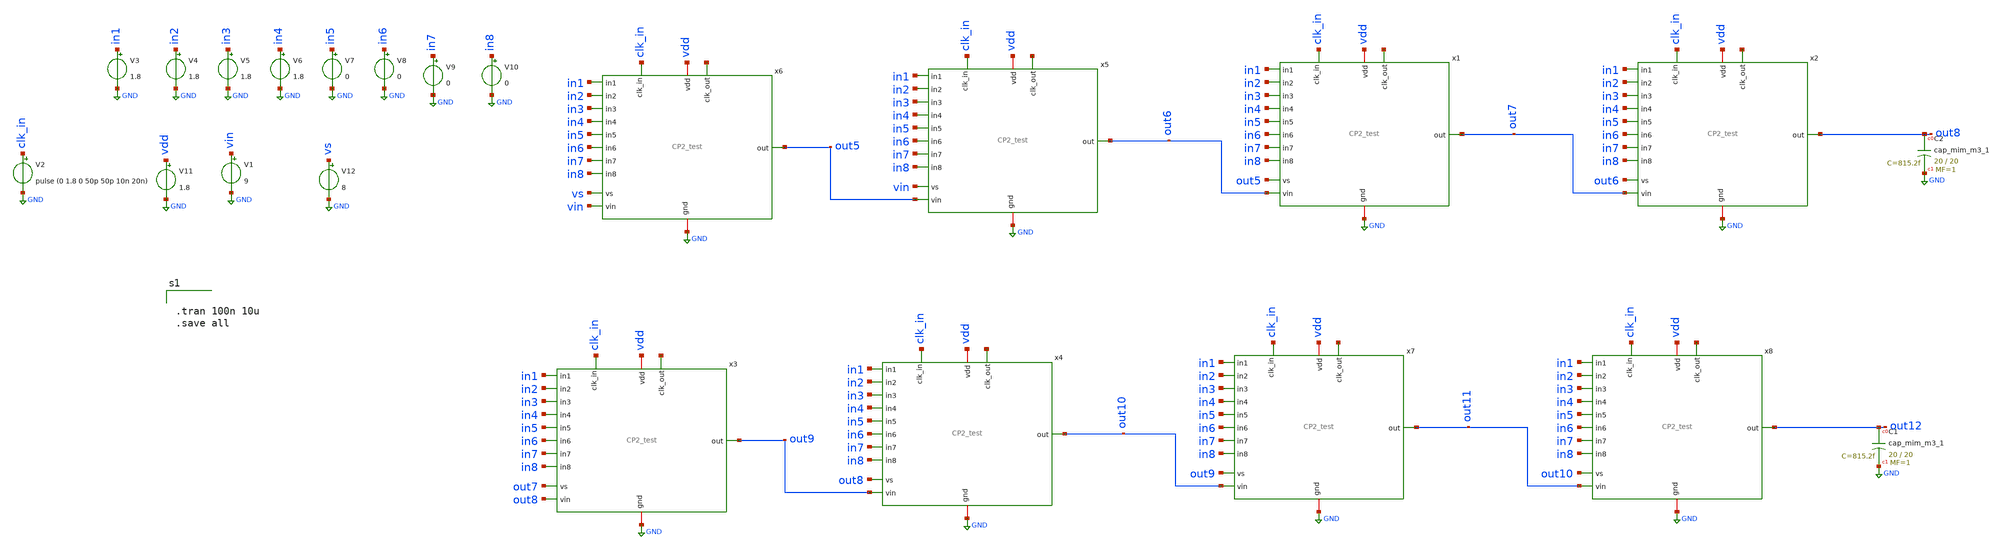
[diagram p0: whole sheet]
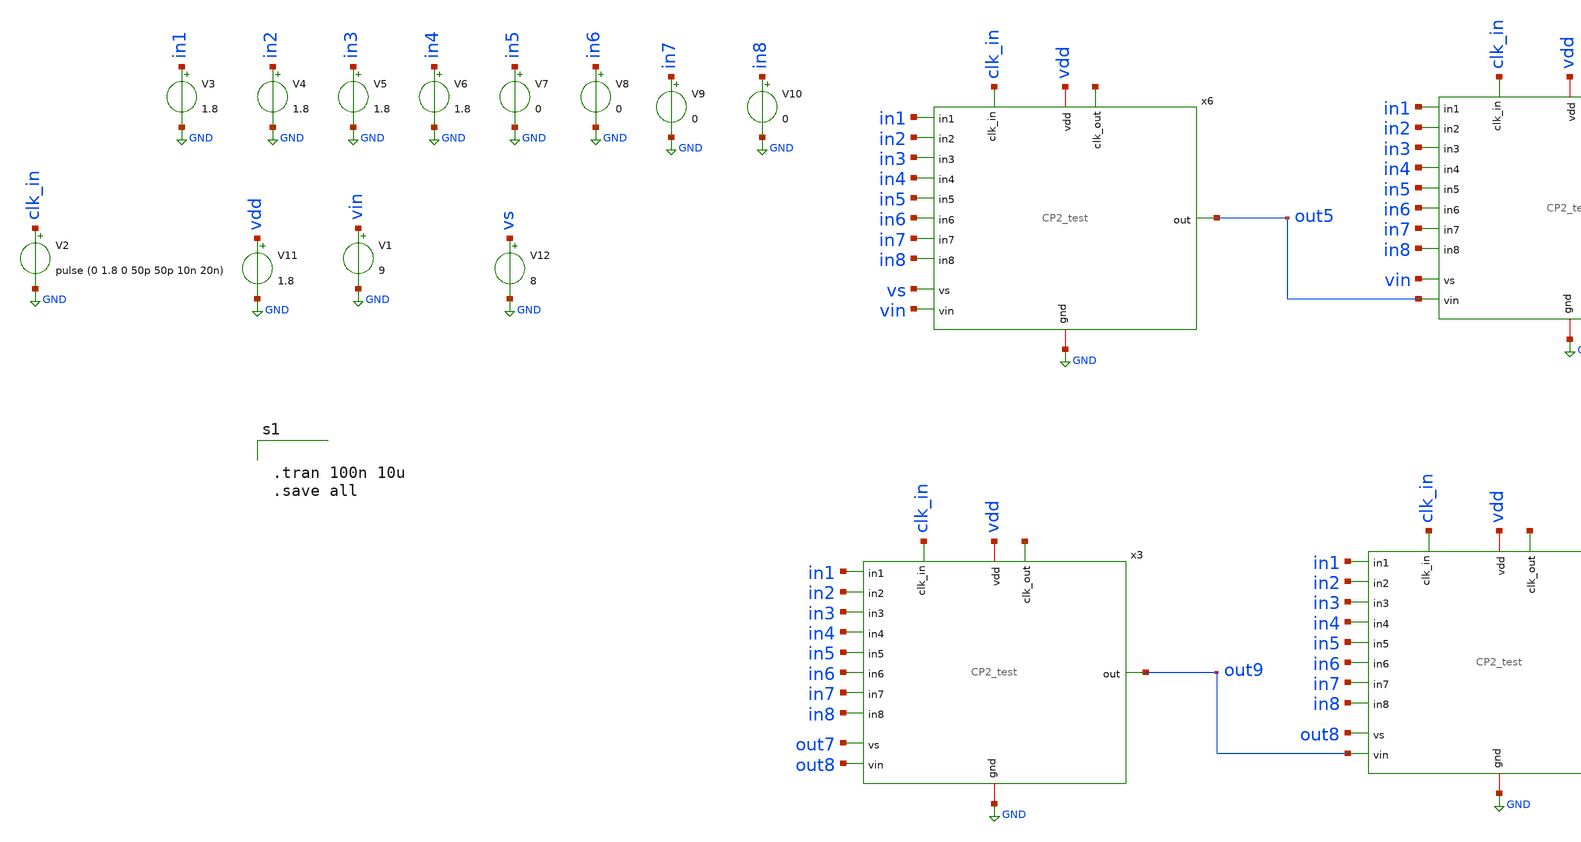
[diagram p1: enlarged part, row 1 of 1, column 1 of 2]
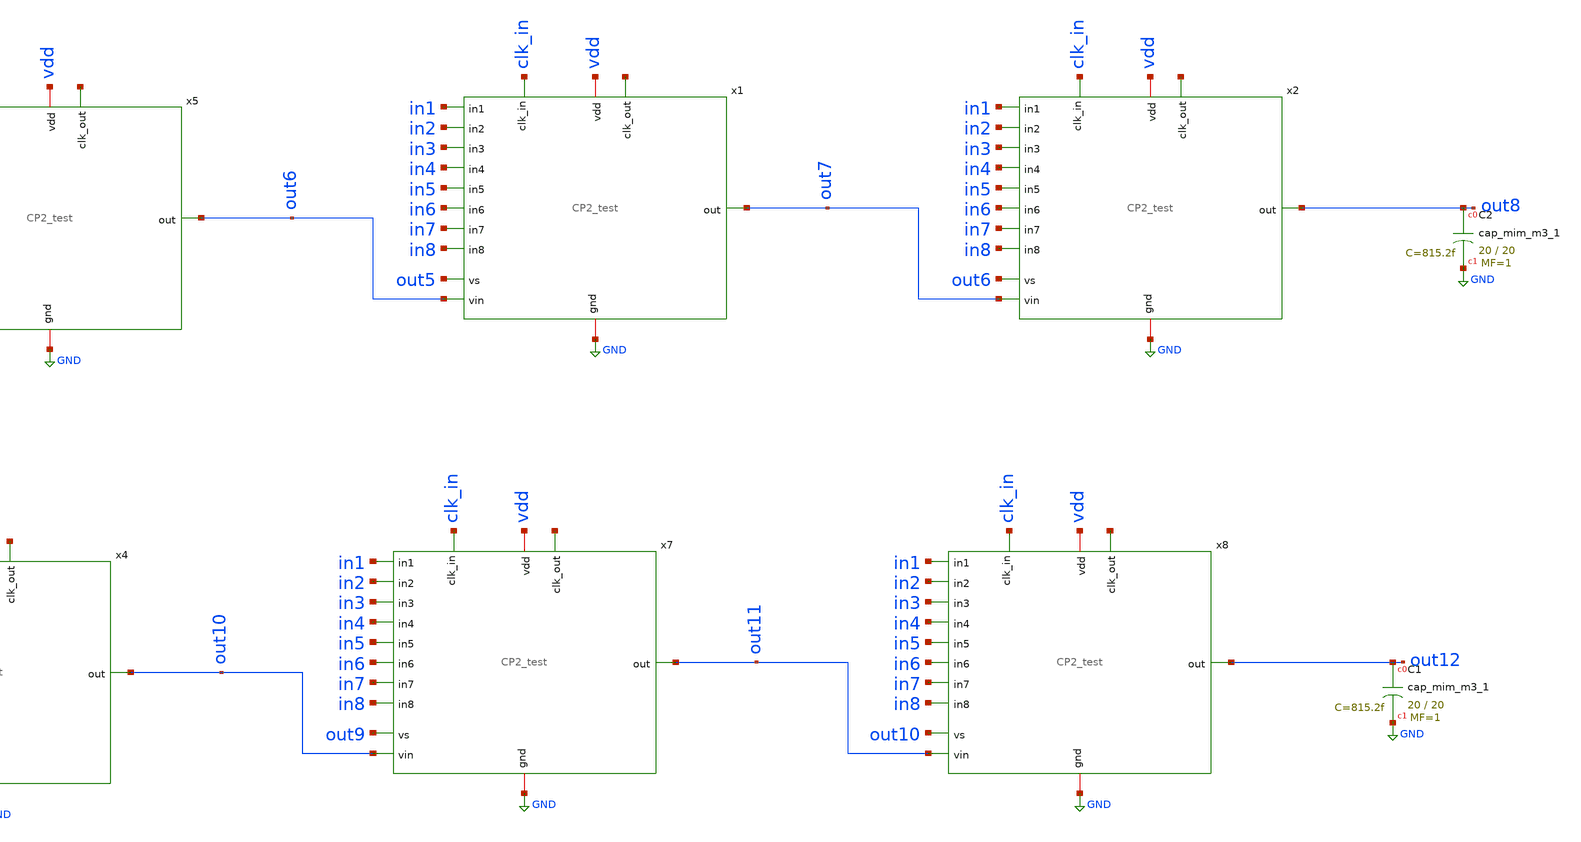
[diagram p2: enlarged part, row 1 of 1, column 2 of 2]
** sch_path: xschem/charge_pumps2/CP2_tb.sch
**.subckt CP2_tb
V1 vin GND 9
V2 clk_in GND pulse (0 1.8 0 50p 50p 10n 20n)
V3 in1 GND 1.8
V4 in2 GND 1.8
V5 in3 GND 1.8
V6 in4 GND 1.8
V7 in5 GND 0
V8 in6 GND 0
V9 in7 GND 0
V10 in8 GND 0
V11 vdd GND 1.8
x6 GND vs clk_in vin out5 in1 in2 in3 in4 in5 in6 in7 in8 vdd net1 CP2_test
x5 GND vin clk_in out5 out6 in1 in2 in3 in4 in5 in6 in7 in8 vdd net2 CP2_test
V12 vs GND 8
x1 GND out5 clk_in out6 out7 in1 in2 in3 in4 in5 in6 in7 in8 vdd net3 CP2_test
x2 GND out6 clk_in out7 out8 in1 in2 in3 in4 in5 in6 in7 in8 vdd net4 CP2_test
XC2 out8 GND sky130_fd_pr__cap_mim_m3_1 W=20 L=20 MF=1 m=1
x3 GND out7 clk_in out8 out9 in1 in2 in3 in4 in5 in6 in7 in8 vdd net5 CP2_test
x4 GND out8 clk_in out9 out10 in1 in2 in3 in4 in5 in6 in7 in8 vdd net6 CP2_test
x7 GND out9 clk_in out10 out11 in1 in2 in3 in4 in5 in6 in7 in8 vdd net7 CP2_test
x8 GND out10 clk_in out11 out12 in1 in2 in3 in4 in5 in6 in7 in8 vdd net8 CP2_test
XC1 out12 GND sky130_fd_pr__cap_mim_m3_1 W=20 L=20 MF=1 m=1
**** begin user architecture code

** opencircuitdesign pdks install
.lib $::SKYWATER_MODELS/sky130.lib.spice tt




.tran 100n 10u
.save all


**** end user architecture code
**.ends
.GLOBAL GND
.end
